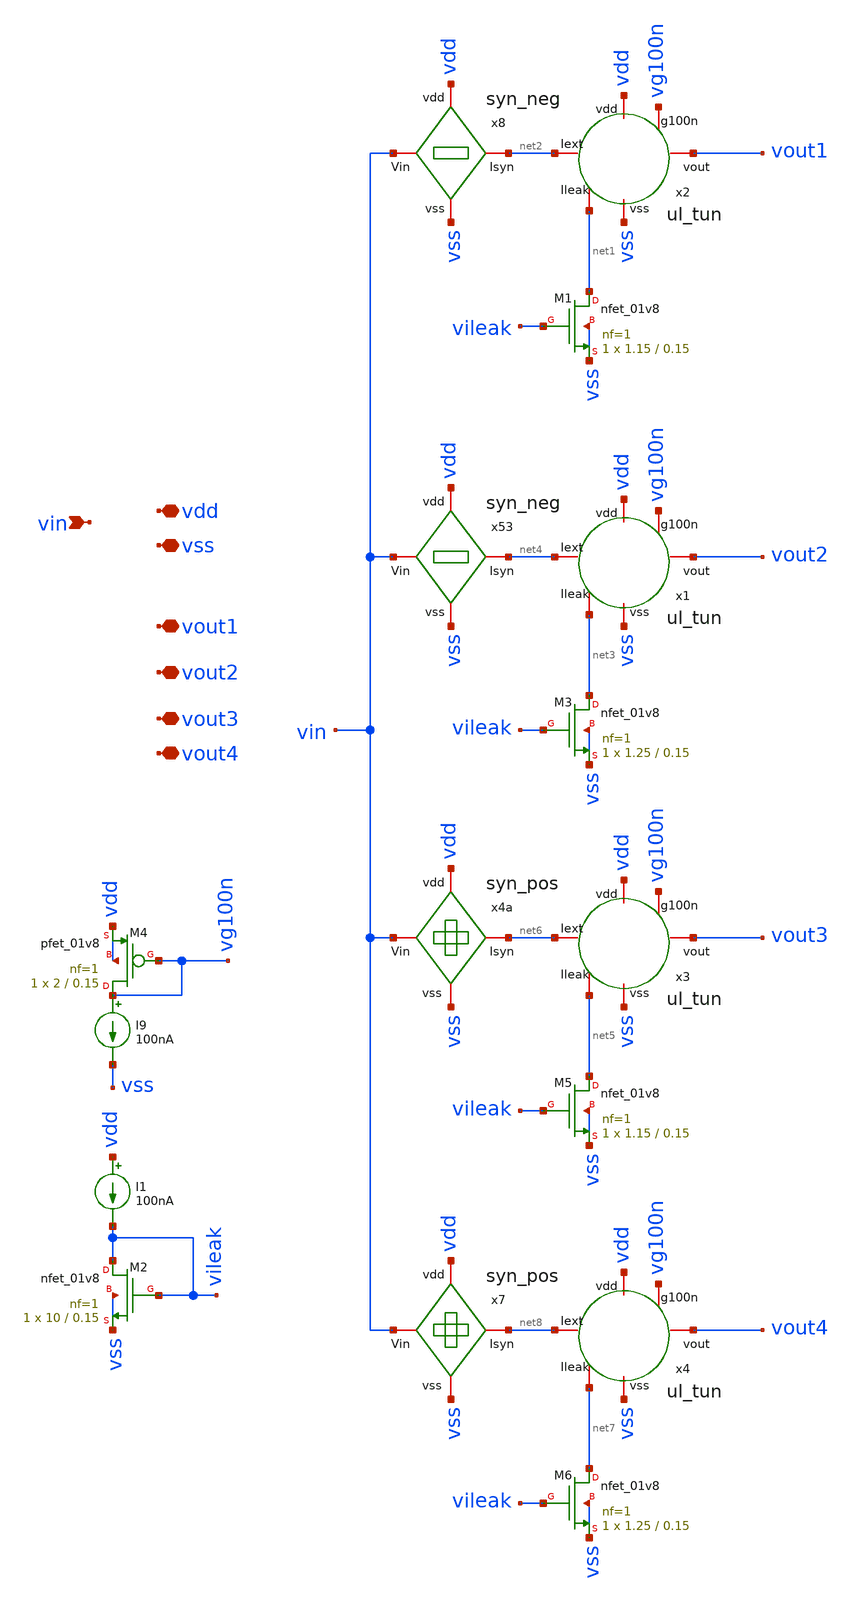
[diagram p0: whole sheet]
** sch_path: layer/layer_input.sch
**.subckt layer_input vdd vss vin vout1 vout2 vout3 vout4
*.iopin vdd
*.iopin vss
*.ipin vin
*.iopin vout1
*.iopin vout2
*.iopin vout3
*.iopin vout4
x2 net2 vdd vg100n vout1 net1 vss ul_tun
x4a vdd vin net6 vss syn_pos
x8 vdd vin net2 vss syn_neg
I9 vg100n vss 100nA
XM4 vg100n vg100n vdd vdd sky130_fd_pr__pfet_01v8 L=0.15 W=2 nf=1 ad='int((nf+1)/2) * W/nf * 0.29' as='int((nf+2)/2) * W/nf * 0.29'
+ pd='2*int((nf+1)/2) * (W/nf + 0.29)' ps='2*int((nf+2)/2) * (W/nf + 0.29)' nrd='0.29 / W' nrs='0.29 / W'
+ sa=0 sb=0 sd=0 mult=1 m=1
XM1 net1 vileak vss vss sky130_fd_pr__nfet_01v8 L=0.15 W=1.15 nf=1 ad='int((nf+1)/2) * W/nf * 0.29' as='int((nf+2)/2) * W/nf * 0.29'
+ pd='2*int((nf+1)/2) * (W/nf + 0.29)' ps='2*int((nf+2)/2) * (W/nf + 0.29)' nrd='0.29 / W' nrs='0.29 / W'
+ sa=0 sb=0 sd=0 mult=1 m=1
XM2 vileak vileak vss vss sky130_fd_pr__nfet_01v8 L=0.15 W=10 nf=1 ad='int((nf+1)/2) * W/nf * 0.29' as='int((nf+2)/2) * W/nf * 0.29'
+ pd='2*int((nf+1)/2) * (W/nf + 0.29)' ps='2*int((nf+2)/2) * (W/nf + 0.29)' nrd='0.29 / W' nrs='0.29 / W'
+ sa=0 sb=0 sd=0 mult=1 m=1
I1 vdd vileak 100nA
x1 net4 vdd vg100n vout2 net3 vss ul_tun
x53 vdd vin net4 vss syn_neg
XM3 net3 vileak vss vss sky130_fd_pr__nfet_01v8 L=0.15 W=1.25 nf=1 ad='int((nf+1)/2) * W/nf * 0.29' as='int((nf+2)/2) * W/nf * 0.29'
+ pd='2*int((nf+1)/2) * (W/nf + 0.29)' ps='2*int((nf+2)/2) * (W/nf + 0.29)' nrd='0.29 / W' nrs='0.29 / W'
+ sa=0 sb=0 sd=0 mult=1 m=1
x3 net6 vdd vg100n vout3 net5 vss ul_tun
XM5 net5 vileak vss vss sky130_fd_pr__nfet_01v8 L=0.15 W=1.15 nf=1 ad='int((nf+1)/2) * W/nf * 0.29' as='int((nf+2)/2) * W/nf * 0.29'
+ pd='2*int((nf+1)/2) * (W/nf + 0.29)' ps='2*int((nf+2)/2) * (W/nf + 0.29)' nrd='0.29 / W' nrs='0.29 / W'
+ sa=0 sb=0 sd=0 mult=1 m=1
x7 vdd vin net8 vss syn_pos
x4 net8 vdd vg100n vout4 net7 vss ul_tun
XM6 net7 vileak vss vss sky130_fd_pr__nfet_01v8 L=0.15 W=1.25 nf=1 ad='int((nf+1)/2) * W/nf * 0.29' as='int((nf+2)/2) * W/nf * 0.29'
+ pd='2*int((nf+1)/2) * (W/nf + 0.29)' ps='2*int((nf+2)/2) * (W/nf + 0.29)' nrd='0.29 / W' nrs='0.29 / W'
+ sa=0 sb=0 sd=0 mult=1 m=1
**.ends

* expanding   symbol:  Neuron/ultralif/ul_tun.sym # of pins=6
** sym_path: Neuron/ultralif/ul_tun.sym
** sch_path: Neuron/ultralif/ul_tun.sch
.subckt ul_tun Iext vdd g100n vout Ileak vss
*.iopin Iext
*.iopin vout
*.iopin vss
*.iopin Ileak
*.iopin vdd
*.iopin g100n
XM1 Ileak Ileak net1 vdd sky130_fd_pr__pfet_01v8 L=10 W=1 nf=1 ad='int((nf+1)/2) * W/nf * 0.29' as='int((nf+2)/2) * W/nf * 0.29'
+ pd='2*int((nf+1)/2) * (W/nf + 0.29)' ps='2*int((nf+2)/2) * (W/nf + 0.29)' nrd='0.29 / W' nrs='0.29 / W'
+ sa=0 sb=0 sd=0 mult=1 m=1
XM2 Ileak net2 net1 vdd sky130_fd_pr__pfet_01v8 L=0.15 W=1.5 nf=1 ad='int((nf+1)/2) * W/nf * 0.29' as='int((nf+2)/2) * W/nf * 0.29'
+ pd='2*int((nf+1)/2) * (W/nf + 0.29)' ps='2*int((nf+2)/2) * (W/nf + 0.29)' nrd='0.29 / W' nrs='0.29 / W'
+ sa=0 sb=0 sd=0 mult=1 m=1
XM3 net2 net2 net1 vdd sky130_fd_pr__pfet_01v8 L=0.15 W=15 nf=1 ad='int((nf+1)/2) * W/nf * 0.29' as='int((nf+2)/2) * W/nf * 0.29'
+ pd='2*int((nf+1)/2) * (W/nf + 0.29)' ps='2*int((nf+2)/2) * (W/nf + 0.29)' nrd='0.29 / W' nrs='0.29 / W'
+ sa=0 sb=0 sd=0 mult=1 m=1
XM4 net2 Ileak vss vss sky130_fd_pr__nfet_01v8 L=4 W=1 nf=1 ad='int((1 + 1)/2) * 1 / 1 * 0.29' as='int((1 + 2)/2) * 1 / 1 * 0.29'
+ pd='2*int((1 + 1)/2) * (1 / 1 + 0.29)' ps='2*int((1 + 2)/2) * (1 / 1 + 0.29)' nrd='0.29 / 1 ' nrs='0.29 / 1 '
+ sa=0 sb=0 sd=0 mult=1 m=1
C1 net1 vss 1p m=1
XM5 vout_n Ileak vss vss sky130_fd_pr__nfet_01v8 L=0.15 W=1 nf=1 ad='int((1 + 1)/2) * 1 / 1 * 0.29' as='int((1 + 2)/2) * 1 / 1 * 0.29'
+ pd='2*int((1 + 1)/2) * (1 / 1 + 0.29)' ps='2*int((1 + 2)/2) * (1 / 1 + 0.29)' nrd='0.29 / 1 ' nrs='0.29 / 1 '
+ sa=0 sb=0 sd=0 mult=1 m=1
XM6 vout_n g100n vdd vdd sky130_fd_pr__pfet_01v8 L=0.15 W=2 nf=1 ad='int((nf+1)/2) * W/nf * 0.29' as='int((nf+2)/2) * W/nf * 0.29'
+ pd='2*int((nf+1)/2) * (W/nf + 0.29)' ps='2*int((nf+2)/2) * (W/nf + 0.29)' nrd='0.29 / W' nrs='0.29 / W'
+ sa=0 sb=0 sd=0 mult=1 m=1
XM7 vout vout_n vss vss sky130_fd_pr__nfet_01v8 L=0.15 W=1 nf=1 ad='int((1 + 1)/2) * 1 / 1 * 0.29' as='int((1 + 2)/2) * 1 / 1 * 0.29'
+ pd='2*int((1 + 1)/2) * (1 / 1 + 0.29)' ps='2*int((1 + 2)/2) * (1 / 1 + 0.29)' nrd='0.29 / 1 ' nrs='0.29 / 1 '
+ sa=0 sb=0 sd=0 mult=1 m=1
XM8 vout vout_n vdd vdd sky130_fd_pr__pfet_01v8 L=0.15 W=2 nf=1 ad='int((nf+1)/2) * W/nf * 0.29' as='int((nf+2)/2) * W/nf * 0.29'
+ pd='2*int((nf+1)/2) * (W/nf + 0.29)' ps='2*int((nf+2)/2) * (W/nf + 0.29)' nrd='0.29 / W' nrs='0.29 / W'
+ sa=0 sb=0 sd=0 mult=1 m=1
XM9 net3 Ileak Iext vdd sky130_fd_pr__pfet_01v8 L=0.15 W=2 nf=1 ad='int((nf+1)/2) * W/nf * 0.29' as='int((nf+2)/2) * W/nf * 0.29'
+ pd='2*int((nf+1)/2) * (W/nf + 0.29)' ps='2*int((nf+2)/2) * (W/nf + 0.29)' nrd='0.29 / W' nrs='0.29 / W'
+ sa=0 sb=0 sd=0 mult=1 m=1
vext net3 net1 0
**** begin user architecture code


.save i(vext)


**** end user architecture code
.ends


* expanding   symbol:  Neuron/ultralif/syn_pos.sym # of pins=4
** sym_path: Neuron/ultralif/syn_pos.sym
** sch_path: Neuron/ultralif/syn_pos.sch
.subckt syn_pos vdd Vin Isyn vss
*.iopin Vin
*.iopin vdd
*.iopin vss
*.iopin Isyn
XM9 Isyn vx vdd vdd sky130_fd_pr__pfet_01v8 L=1 W=0.5 nf=1 ad='int((nf+1)/2) * W/nf * 0.29' as='int((nf+2)/2) * W/nf * 0.29'
+ pd='2*int((nf+1)/2) * (W/nf + 0.29)' ps='2*int((nf+2)/2) * (W/nf + 0.29)' nrd='0.29 / W' nrs='0.29 / W'
+ sa=0 sb=0 sd=0 mult=1 m=1
XM10 vx vx vdd vdd sky130_fd_pr__pfet_01v8 L=0.15 W=0.5 nf=1 ad='int((nf+1)/2) * W/nf * 0.29' as='int((nf+2)/2) * W/nf * 0.29'
+ pd='2*int((nf+1)/2) * (W/nf + 0.29)' ps='2*int((nf+2)/2) * (W/nf + 0.29)' nrd='0.29 / W' nrs='0.29 / W'
+ sa=0 sb=0 sd=0 mult=5 m=5
XM12 vx Vin vss vss sky130_fd_pr__nfet_01v8 L=1 W=0.4 nf=1 ad='int((1 + 1)/2) * 0.4 / 1 * 0.29' as='int((1 + 2)/2) * 0.4 / 1 * 0.29'
+ pd='2*int((1 + 1)/2) * (0.4 / 1 + 0.29)' ps='2*int((1 + 2)/2) * (0.4 / 1 + 0.29)' nrd='0.29 / 0.4 ' nrs='0.29 / 0.4 '
+ sa=0 sb=0 sd=0 mult=1 m=1
.ends


* expanding   symbol:  Neuron/ultralif/syn_neg.sym # of pins=4
** sym_path: Neuron/ultralif/syn_neg.sym
** sch_path: Neuron/ultralif/syn_neg.sch
.subckt syn_neg vdd Vin Isyn vss
*.iopin Vin
*.iopin Isyn
*.iopin vdd
*.iopin vss
XM10 Isyn Vin vx vdd sky130_fd_pr__pfet_01v8 L=35 W=0.5 nf=1 ad='int((nf+1)/2) * W/nf * 0.29' as='int((nf+2)/2) * W/nf * 0.29'
+ pd='2*int((nf+1)/2) * (W/nf + 0.29)' ps='2*int((nf+2)/2) * (W/nf + 0.29)' nrd='0.29 / W' nrs='0.29 / W'
+ sa=0 sb=0 sd=0 mult=1 m=1
XM1 vx Vin vdd vdd sky130_fd_pr__pfet_01v8 L=35 W=0.5 nf=1 ad='int((nf+1)/2) * W/nf * 0.29' as='int((nf+2)/2) * W/nf * 0.29'
+ pd='2*int((nf+1)/2) * (W/nf + 0.29)' ps='2*int((nf+2)/2) * (W/nf + 0.29)' nrd='0.29 / W' nrs='0.29 / W'
+ sa=0 sb=0 sd=0 mult=1 m=1
XM2 Isyn net1 vdd vdd sky130_fd_pr__pfet_01v8 L=1 W=0.5 nf=1 ad='int((nf+1)/2) * W/nf * 0.29' as='int((nf+2)/2) * W/nf * 0.29'
+ pd='2*int((nf+1)/2) * (W/nf + 0.29)' ps='2*int((nf+2)/2) * (W/nf + 0.29)' nrd='0.29 / W' nrs='0.29 / W'
+ sa=0 sb=0 sd=0 mult=1 m=1
XR1 net1 vdd sky130_fd_pr__res_generic_po W=1.15 L=1 m=1
XR2 vss net1 sky130_fd_pr__res_generic_po W=1 L=1 m=1
.ends

.end
